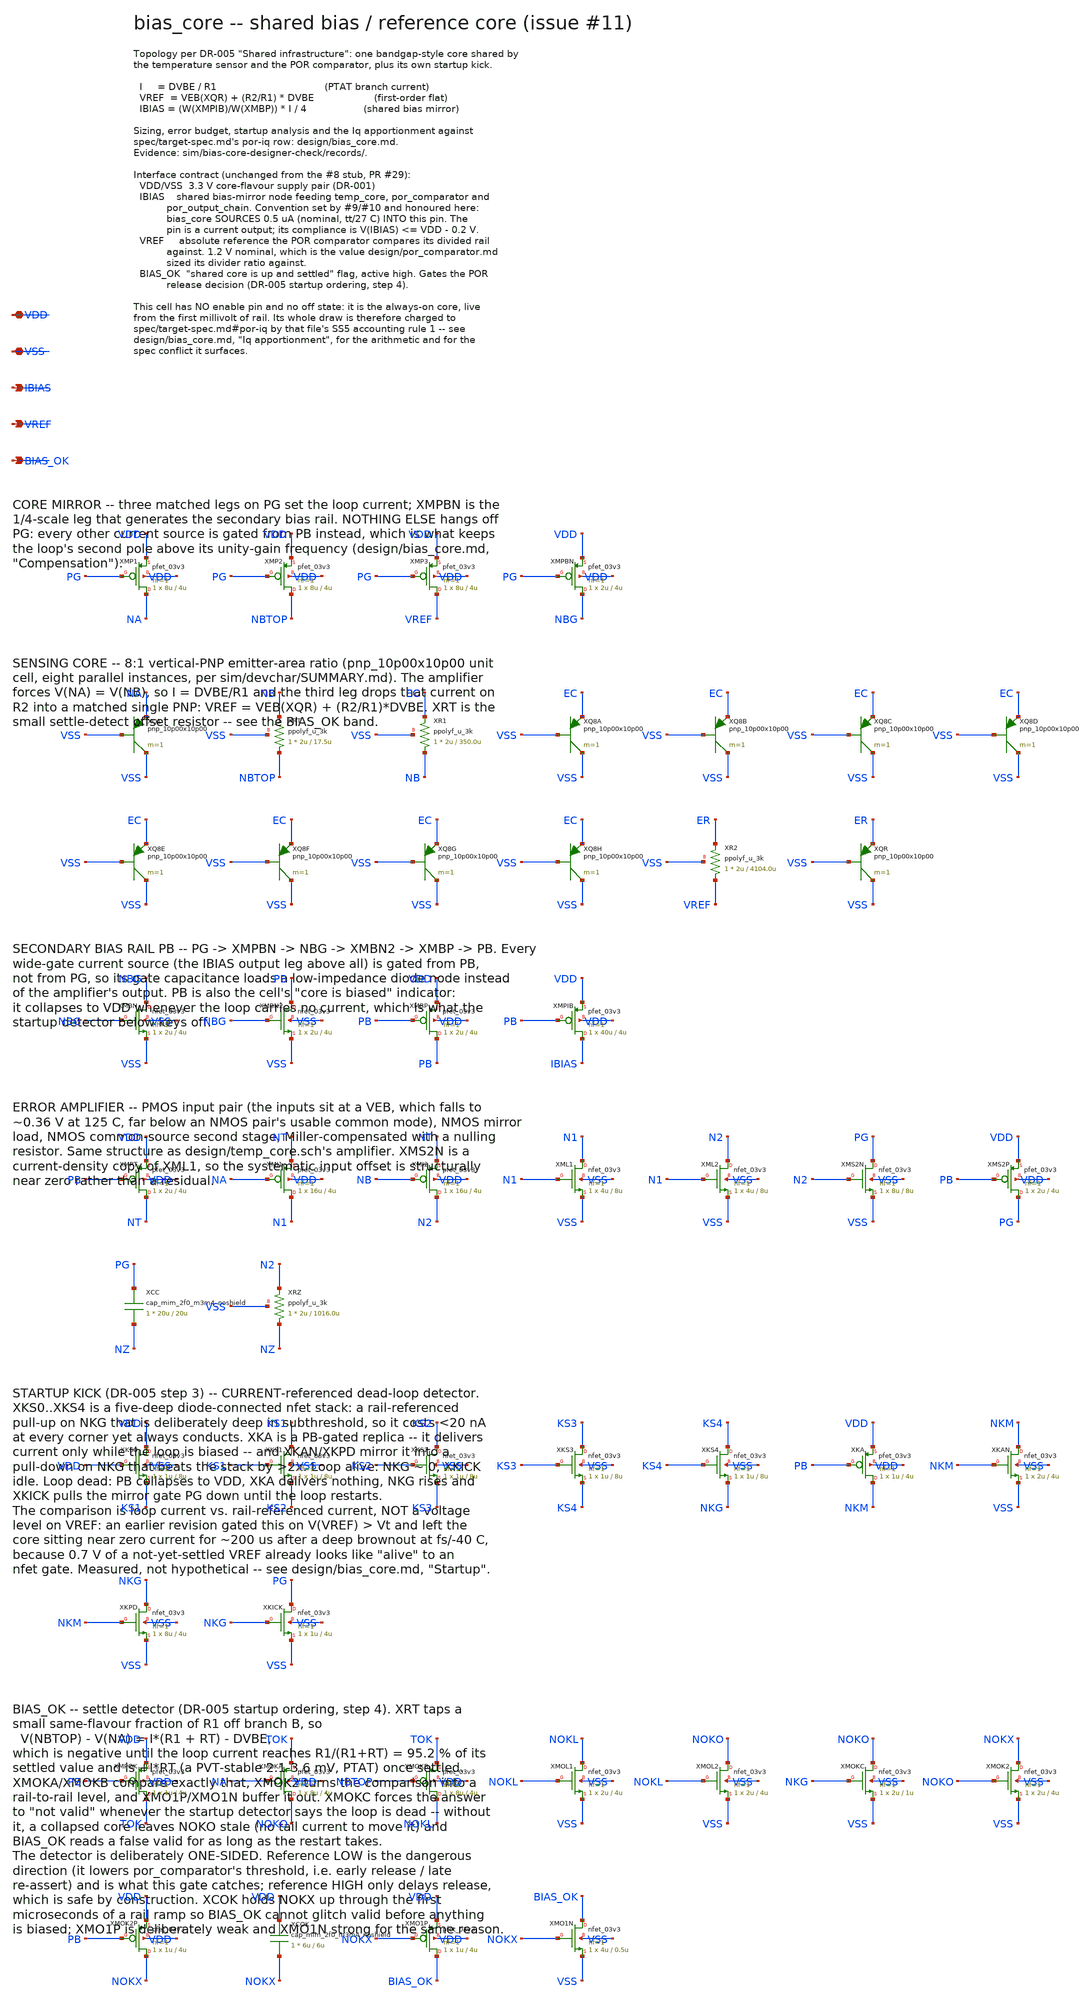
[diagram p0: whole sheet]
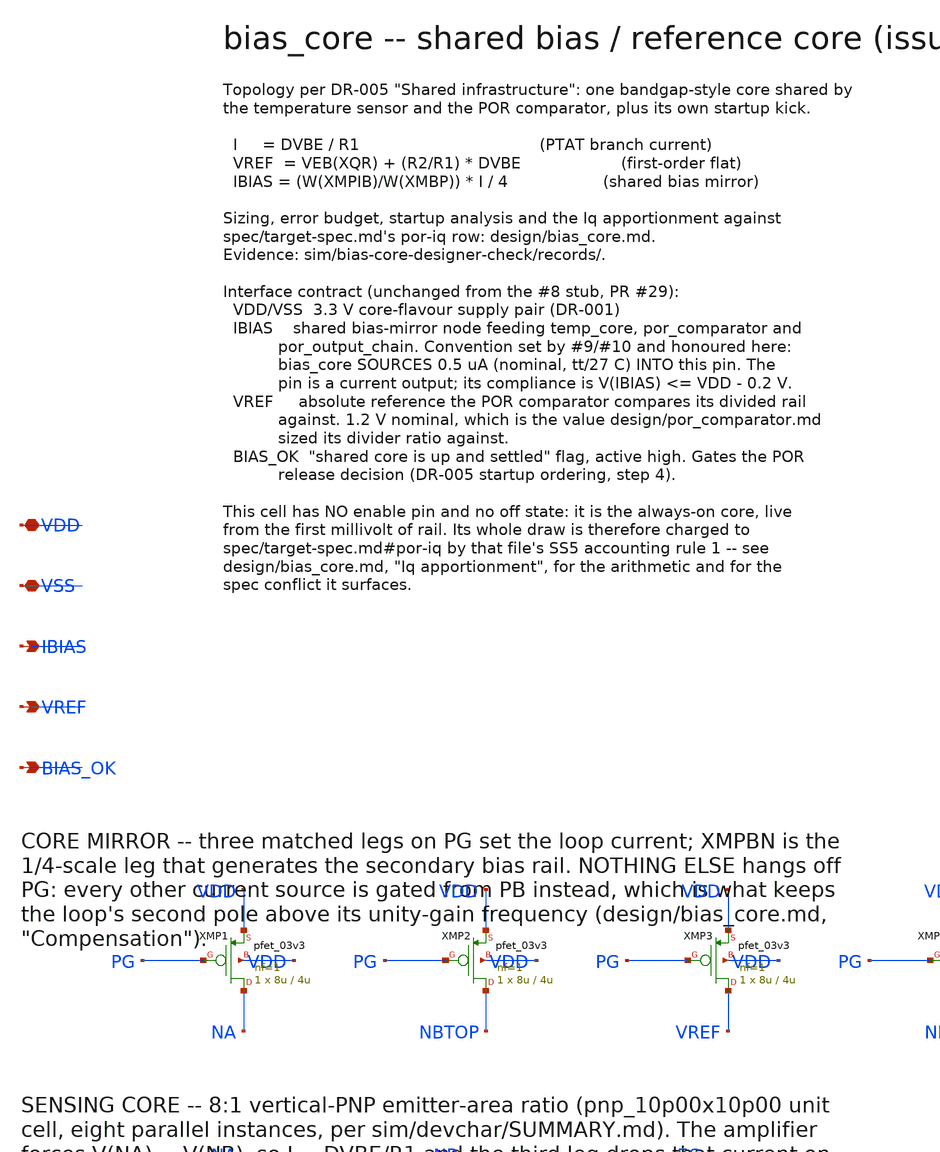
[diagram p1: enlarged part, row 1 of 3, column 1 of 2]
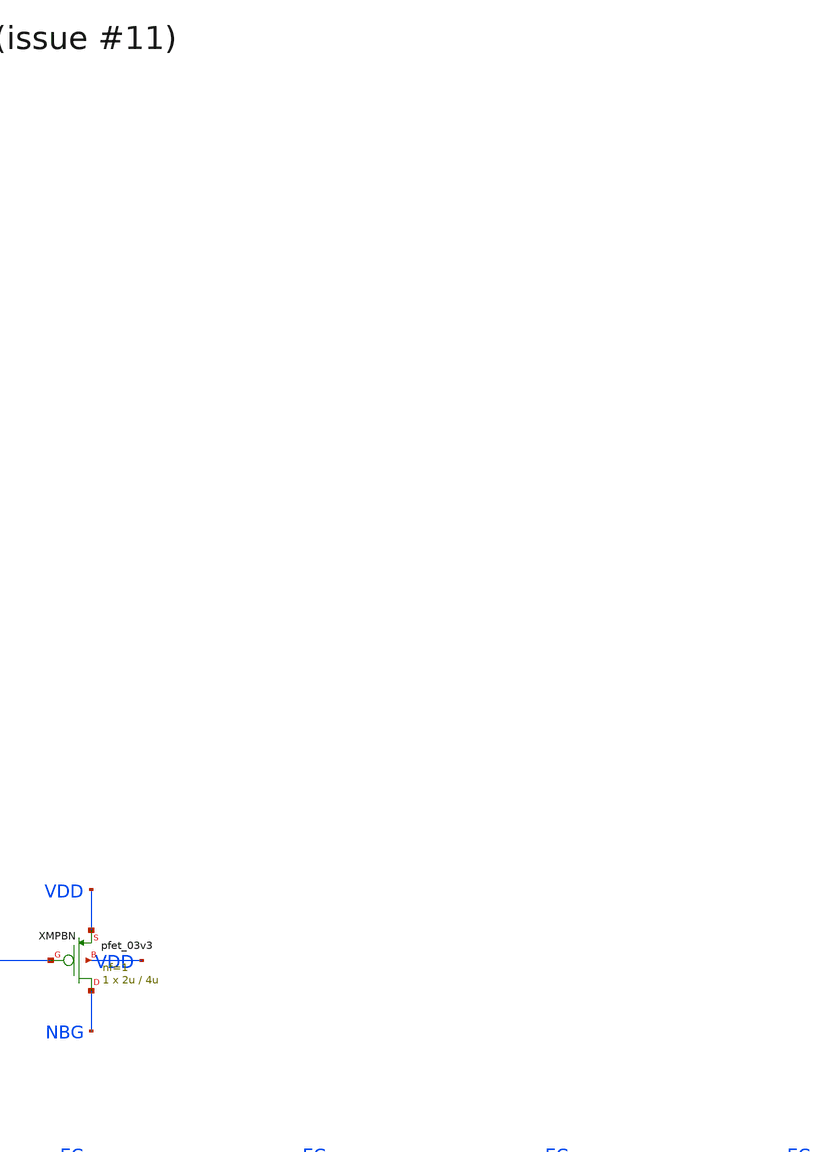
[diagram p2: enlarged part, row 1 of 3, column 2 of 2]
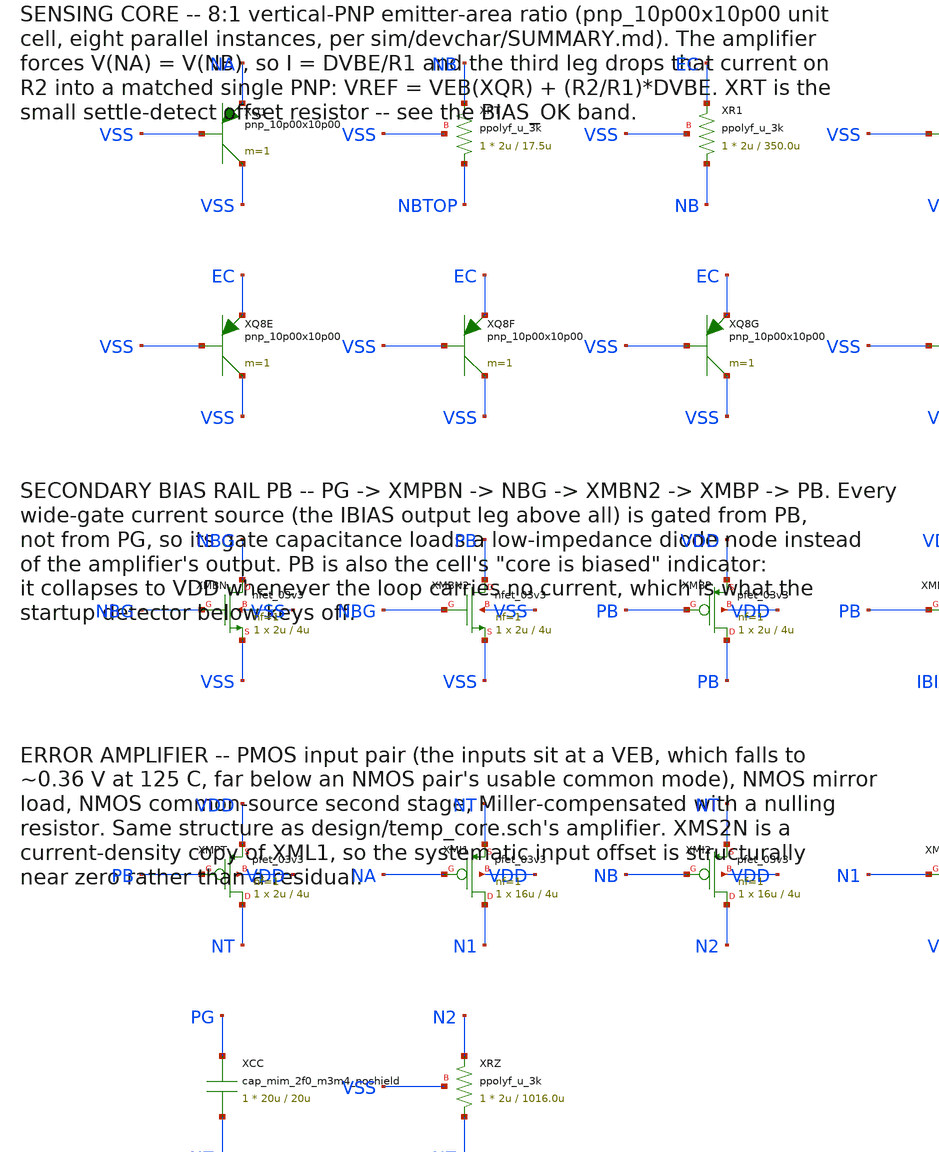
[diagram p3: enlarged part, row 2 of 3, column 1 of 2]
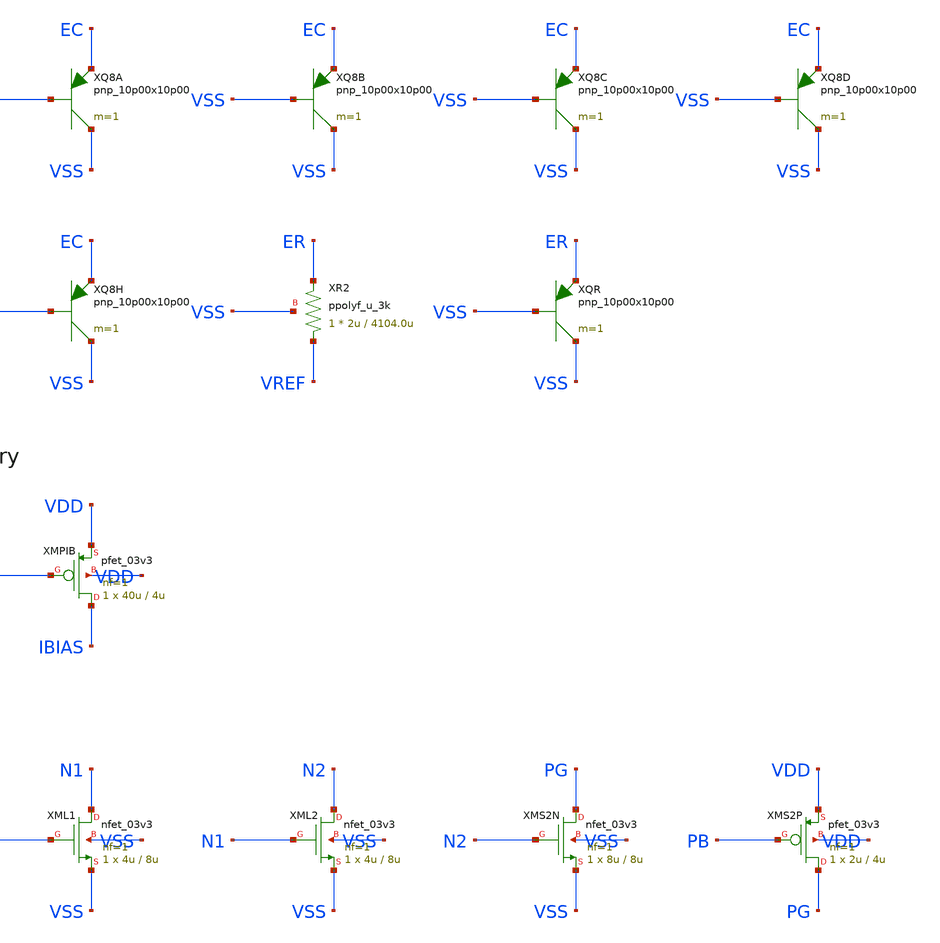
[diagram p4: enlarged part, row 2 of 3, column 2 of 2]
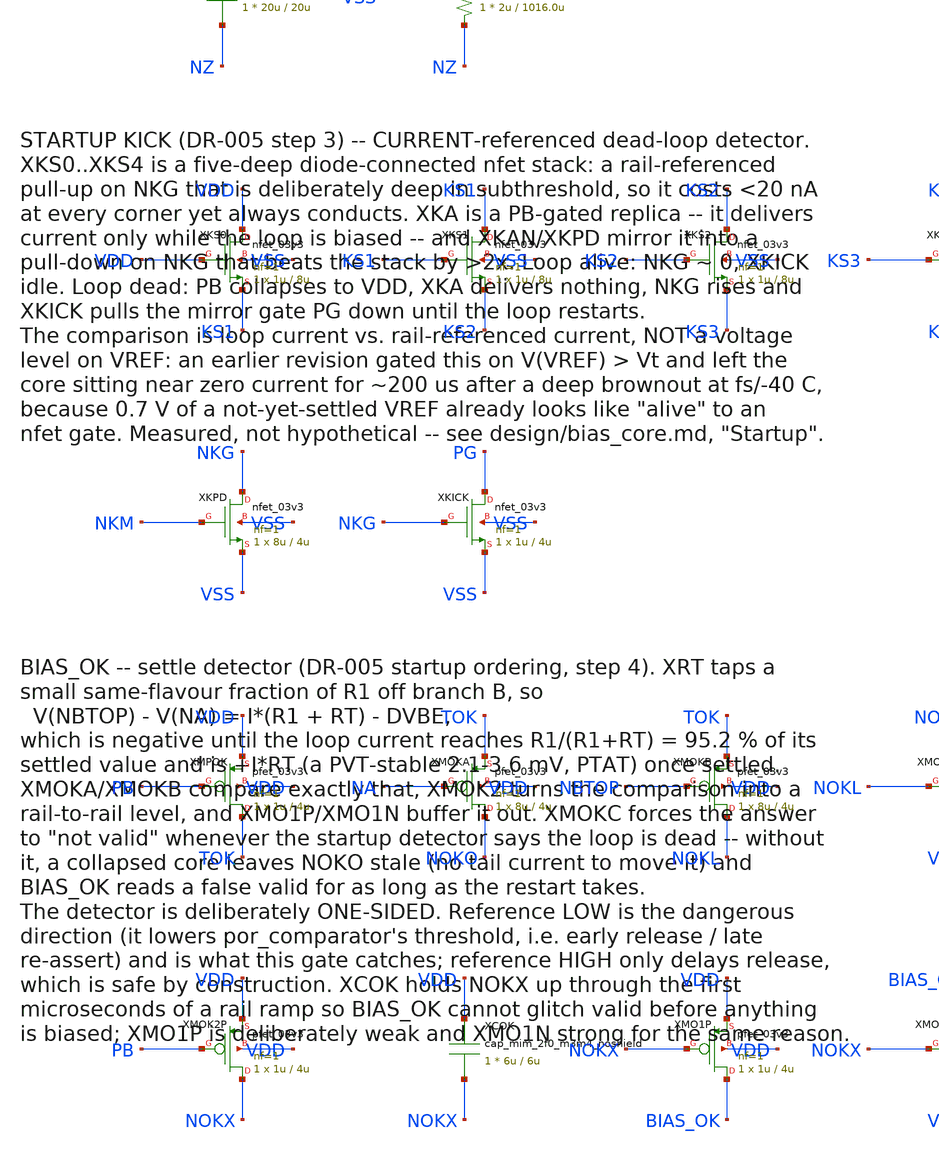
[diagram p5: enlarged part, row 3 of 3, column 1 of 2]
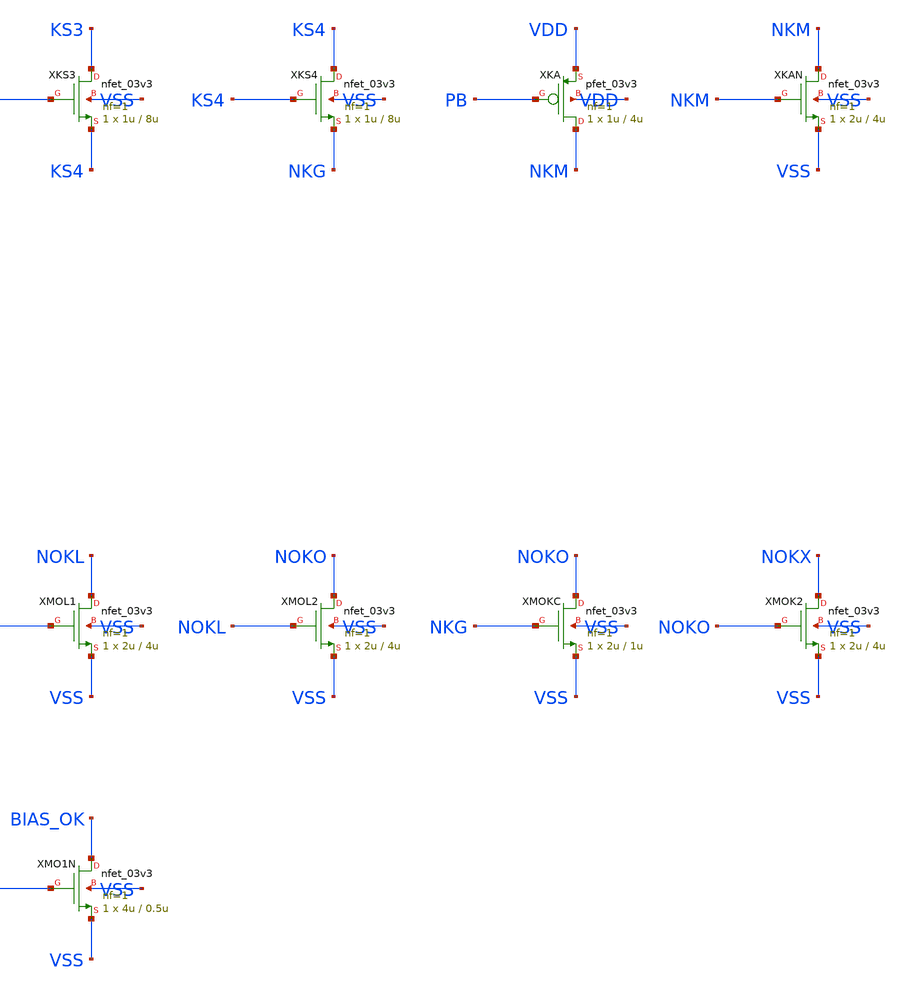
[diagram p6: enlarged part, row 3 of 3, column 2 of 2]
** sch_path: design/bias_core.sch
**.subckt bias_core VDD VSS IBIAS VREF BIAS_OK
*.iopin VDD
*.iopin VSS
*.opin IBIAS
*.opin VREF
*.opin BIAS_OK
XMP1 NA PG VDD VDD pfet_03v3 L=4u W=8u nf=1 ad='int((nf+1)/2) * W/nf * 0.18u' as='int((nf+2)/2) * W/nf * 0.18u'
+ pd='2*int((nf+1)/2) * (W/nf + 0.18u)' ps='2*int((nf+2)/2) * (W/nf + 0.18u)' nrd='0.18u / W' nrs='0.18u / W'
+ sa=0 sb=0 sd=0 m=1
XMP2 NBTOP PG VDD VDD pfet_03v3 L=4u W=8u nf=1 ad='int((nf+1)/2) * W/nf * 0.18u' as='int((nf+2)/2) * W/nf * 0.18u'
+ pd='2*int((nf+1)/2) * (W/nf + 0.18u)' ps='2*int((nf+2)/2) * (W/nf + 0.18u)' nrd='0.18u / W' nrs='0.18u / W'
+ sa=0 sb=0 sd=0 m=1
XMP3 VREF PG VDD VDD pfet_03v3 L=4u W=8u nf=1 ad='int((nf+1)/2) * W/nf * 0.18u' as='int((nf+2)/2) * W/nf * 0.18u'
+ pd='2*int((nf+1)/2) * (W/nf + 0.18u)' ps='2*int((nf+2)/2) * (W/nf + 0.18u)' nrd='0.18u / W' nrs='0.18u / W'
+ sa=0 sb=0 sd=0 m=1
XMPBN NBG PG VDD VDD pfet_03v3 L=4u W=2u nf=1 ad='int((nf+1)/2) * W/nf * 0.18u' as='int((nf+2)/2) * W/nf * 0.18u'
+ pd='2*int((nf+1)/2) * (W/nf + 0.18u)' ps='2*int((nf+2)/2) * (W/nf + 0.18u)' nrd='0.18u / W' nrs='0.18u / W'
+ sa=0 sb=0 sd=0 m=1
XQ1 VSS VSS NA pnp_10p00x10p00 m=1
XRT NBTOP NB VSS ppolyf_u_3k r_width=2u r_length=17.5u m=1
XR1 NB EC VSS ppolyf_u_3k r_width=2u r_length=350.0u m=1
XQ8A VSS VSS EC pnp_10p00x10p00 m=1
XQ8B VSS VSS EC pnp_10p00x10p00 m=1
XQ8C VSS VSS EC pnp_10p00x10p00 m=1
XQ8D VSS VSS EC pnp_10p00x10p00 m=1
XQ8E VSS VSS EC pnp_10p00x10p00 m=1
XQ8F VSS VSS EC pnp_10p00x10p00 m=1
XQ8G VSS VSS EC pnp_10p00x10p00 m=1
XQ8H VSS VSS EC pnp_10p00x10p00 m=1
XR2 VREF ER VSS ppolyf_u_3k r_width=2u r_length=4104.0u m=1
XQR VSS VSS ER pnp_10p00x10p00 m=1
XMBN NBG NBG VSS VSS nfet_03v3 L=4u W=2u nf=1 ad='int((nf+1)/2) * W/nf * 0.18u' as='int((nf+2)/2) * W/nf * 0.18u'
+ pd='2*int((nf+1)/2) * (W/nf + 0.18u)' ps='2*int((nf+2)/2) * (W/nf + 0.18u)' nrd='0.18u / W' nrs='0.18u / W'
+ sa=0 sb=0 sd=0 m=1
XMBN2 PB NBG VSS VSS nfet_03v3 L=4u W=2u nf=1 ad='int((nf+1)/2) * W/nf * 0.18u' as='int((nf+2)/2) * W/nf * 0.18u'
+ pd='2*int((nf+1)/2) * (W/nf + 0.18u)' ps='2*int((nf+2)/2) * (W/nf + 0.18u)' nrd='0.18u / W' nrs='0.18u / W'
+ sa=0 sb=0 sd=0 m=1
XMBP PB PB VDD VDD pfet_03v3 L=4u W=2u nf=1 ad='int((nf+1)/2) * W/nf * 0.18u' as='int((nf+2)/2) * W/nf * 0.18u'
+ pd='2*int((nf+1)/2) * (W/nf + 0.18u)' ps='2*int((nf+2)/2) * (W/nf + 0.18u)' nrd='0.18u / W' nrs='0.18u / W'
+ sa=0 sb=0 sd=0 m=1
XMPIB IBIAS PB VDD VDD pfet_03v3 L=4u W=40u nf=1 ad='int((nf+1)/2) * W/nf * 0.18u' as='int((nf+2)/2) * W/nf * 0.18u'
+ pd='2*int((nf+1)/2) * (W/nf + 0.18u)' ps='2*int((nf+2)/2) * (W/nf + 0.18u)' nrd='0.18u / W' nrs='0.18u / W'
+ sa=0 sb=0 sd=0 m=1
XMPT NT PB VDD VDD pfet_03v3 L=4u W=2u nf=1 ad='int((nf+1)/2) * W/nf * 0.18u' as='int((nf+2)/2) * W/nf * 0.18u'
+ pd='2*int((nf+1)/2) * (W/nf + 0.18u)' ps='2*int((nf+2)/2) * (W/nf + 0.18u)' nrd='0.18u / W' nrs='0.18u / W'
+ sa=0 sb=0 sd=0 m=1
XMI1 N1 NA NT VDD pfet_03v3 L=4u W=16u nf=1 ad='int((nf+1)/2) * W/nf * 0.18u' as='int((nf+2)/2) * W/nf * 0.18u'
+ pd='2*int((nf+1)/2) * (W/nf + 0.18u)' ps='2*int((nf+2)/2) * (W/nf + 0.18u)' nrd='0.18u / W' nrs='0.18u / W'
+ sa=0 sb=0 sd=0 m=1
XMI2 N2 NB NT VDD pfet_03v3 L=4u W=16u nf=1 ad='int((nf+1)/2) * W/nf * 0.18u' as='int((nf+2)/2) * W/nf * 0.18u'
+ pd='2*int((nf+1)/2) * (W/nf + 0.18u)' ps='2*int((nf+2)/2) * (W/nf + 0.18u)' nrd='0.18u / W' nrs='0.18u / W'
+ sa=0 sb=0 sd=0 m=1
XML1 N1 N1 VSS VSS nfet_03v3 L=8u W=4u nf=1 ad='int((nf+1)/2) * W/nf * 0.18u' as='int((nf+2)/2) * W/nf * 0.18u'
+ pd='2*int((nf+1)/2) * (W/nf + 0.18u)' ps='2*int((nf+2)/2) * (W/nf + 0.18u)' nrd='0.18u / W' nrs='0.18u / W'
+ sa=0 sb=0 sd=0 m=1
XML2 N2 N1 VSS VSS nfet_03v3 L=8u W=4u nf=1 ad='int((nf+1)/2) * W/nf * 0.18u' as='int((nf+2)/2) * W/nf * 0.18u'
+ pd='2*int((nf+1)/2) * (W/nf + 0.18u)' ps='2*int((nf+2)/2) * (W/nf + 0.18u)' nrd='0.18u / W' nrs='0.18u / W'
+ sa=0 sb=0 sd=0 m=1
XMS2N PG N2 VSS VSS nfet_03v3 L=8u W=8u nf=1 ad='int((nf+1)/2) * W/nf * 0.18u' as='int((nf+2)/2) * W/nf * 0.18u'
+ pd='2*int((nf+1)/2) * (W/nf + 0.18u)' ps='2*int((nf+2)/2) * (W/nf + 0.18u)' nrd='0.18u / W' nrs='0.18u / W'
+ sa=0 sb=0 sd=0 m=1
XMS2P PG PB VDD VDD pfet_03v3 L=4u W=2u nf=1 ad='int((nf+1)/2) * W/nf * 0.18u' as='int((nf+2)/2) * W/nf * 0.18u'
+ pd='2*int((nf+1)/2) * (W/nf + 0.18u)' ps='2*int((nf+2)/2) * (W/nf + 0.18u)' nrd='0.18u / W' nrs='0.18u / W'
+ sa=0 sb=0 sd=0 m=1
XCC PG NZ cap_mim_2f0_m3m4_noshield c_width=20u c_length=20u m=1
XRZ NZ N2 VSS ppolyf_u_3k r_width=2u r_length=1016.0u m=1
XKS0 VDD VDD KS1 VSS nfet_03v3 L=8u W=1u nf=1 ad='int((nf+1)/2) * W/nf * 0.18u' as='int((nf+2)/2) * W/nf * 0.18u'
+ pd='2*int((nf+1)/2) * (W/nf + 0.18u)' ps='2*int((nf+2)/2) * (W/nf + 0.18u)' nrd='0.18u / W' nrs='0.18u / W'
+ sa=0 sb=0 sd=0 m=1
XKS1 KS1 KS1 KS2 VSS nfet_03v3 L=8u W=1u nf=1 ad='int((nf+1)/2) * W/nf * 0.18u' as='int((nf+2)/2) * W/nf * 0.18u'
+ pd='2*int((nf+1)/2) * (W/nf + 0.18u)' ps='2*int((nf+2)/2) * (W/nf + 0.18u)' nrd='0.18u / W' nrs='0.18u / W'
+ sa=0 sb=0 sd=0 m=1
XKS2 KS2 KS2 KS3 VSS nfet_03v3 L=8u W=1u nf=1 ad='int((nf+1)/2) * W/nf * 0.18u' as='int((nf+2)/2) * W/nf * 0.18u'
+ pd='2*int((nf+1)/2) * (W/nf + 0.18u)' ps='2*int((nf+2)/2) * (W/nf + 0.18u)' nrd='0.18u / W' nrs='0.18u / W'
+ sa=0 sb=0 sd=0 m=1
XKS3 KS3 KS3 KS4 VSS nfet_03v3 L=8u W=1u nf=1 ad='int((nf+1)/2) * W/nf * 0.18u' as='int((nf+2)/2) * W/nf * 0.18u'
+ pd='2*int((nf+1)/2) * (W/nf + 0.18u)' ps='2*int((nf+2)/2) * (W/nf + 0.18u)' nrd='0.18u / W' nrs='0.18u / W'
+ sa=0 sb=0 sd=0 m=1
XKS4 KS4 KS4 NKG VSS nfet_03v3 L=8u W=1u nf=1 ad='int((nf+1)/2) * W/nf * 0.18u' as='int((nf+2)/2) * W/nf * 0.18u'
+ pd='2*int((nf+1)/2) * (W/nf + 0.18u)' ps='2*int((nf+2)/2) * (W/nf + 0.18u)' nrd='0.18u / W' nrs='0.18u / W'
+ sa=0 sb=0 sd=0 m=1
XKA NKM PB VDD VDD pfet_03v3 L=4u W=1u nf=1 ad='int((nf+1)/2) * W/nf * 0.18u' as='int((nf+2)/2) * W/nf * 0.18u'
+ pd='2*int((nf+1)/2) * (W/nf + 0.18u)' ps='2*int((nf+2)/2) * (W/nf + 0.18u)' nrd='0.18u / W' nrs='0.18u / W'
+ sa=0 sb=0 sd=0 m=1
XKAN NKM NKM VSS VSS nfet_03v3 L=4u W=2u nf=1 ad='int((nf+1)/2) * W/nf * 0.18u' as='int((nf+2)/2) * W/nf * 0.18u'
+ pd='2*int((nf+1)/2) * (W/nf + 0.18u)' ps='2*int((nf+2)/2) * (W/nf + 0.18u)' nrd='0.18u / W' nrs='0.18u / W'
+ sa=0 sb=0 sd=0 m=1
XKPD NKG NKM VSS VSS nfet_03v3 L=4u W=8u nf=1 ad='int((nf+1)/2) * W/nf * 0.18u' as='int((nf+2)/2) * W/nf * 0.18u'
+ pd='2*int((nf+1)/2) * (W/nf + 0.18u)' ps='2*int((nf+2)/2) * (W/nf + 0.18u)' nrd='0.18u / W' nrs='0.18u / W'
+ sa=0 sb=0 sd=0 m=1
XKICK PG NKG VSS VSS nfet_03v3 L=4u W=1u nf=1 ad='int((nf+1)/2) * W/nf * 0.18u' as='int((nf+2)/2) * W/nf * 0.18u'
+ pd='2*int((nf+1)/2) * (W/nf + 0.18u)' ps='2*int((nf+2)/2) * (W/nf + 0.18u)' nrd='0.18u / W' nrs='0.18u / W'
+ sa=0 sb=0 sd=0 m=1
XMPOK TOK PB VDD VDD pfet_03v3 L=4u W=1u nf=1 ad='int((nf+1)/2) * W/nf * 0.18u' as='int((nf+2)/2) * W/nf * 0.18u'
+ pd='2*int((nf+1)/2) * (W/nf + 0.18u)' ps='2*int((nf+2)/2) * (W/nf + 0.18u)' nrd='0.18u / W' nrs='0.18u / W'
+ sa=0 sb=0 sd=0 m=1
XMOKA NOKO NA TOK VDD pfet_03v3 L=4u W=8u nf=1 ad='int((nf+1)/2) * W/nf * 0.18u' as='int((nf+2)/2) * W/nf * 0.18u'
+ pd='2*int((nf+1)/2) * (W/nf + 0.18u)' ps='2*int((nf+2)/2) * (W/nf + 0.18u)' nrd='0.18u / W' nrs='0.18u / W'
+ sa=0 sb=0 sd=0 m=1
XMOKB NOKL NBTOP TOK VDD pfet_03v3 L=4u W=8u nf=1 ad='int((nf+1)/2) * W/nf * 0.18u' as='int((nf+2)/2) * W/nf * 0.18u'
+ pd='2*int((nf+1)/2) * (W/nf + 0.18u)' ps='2*int((nf+2)/2) * (W/nf + 0.18u)' nrd='0.18u / W' nrs='0.18u / W'
+ sa=0 sb=0 sd=0 m=1
XMOL1 NOKL NOKL VSS VSS nfet_03v3 L=4u W=2u nf=1 ad='int((nf+1)/2) * W/nf * 0.18u' as='int((nf+2)/2) * W/nf * 0.18u'
+ pd='2*int((nf+1)/2) * (W/nf + 0.18u)' ps='2*int((nf+2)/2) * (W/nf + 0.18u)' nrd='0.18u / W' nrs='0.18u / W'
+ sa=0 sb=0 sd=0 m=1
XMOL2 NOKO NOKL VSS VSS nfet_03v3 L=4u W=2u nf=1 ad='int((nf+1)/2) * W/nf * 0.18u' as='int((nf+2)/2) * W/nf * 0.18u'
+ pd='2*int((nf+1)/2) * (W/nf + 0.18u)' ps='2*int((nf+2)/2) * (W/nf + 0.18u)' nrd='0.18u / W' nrs='0.18u / W'
+ sa=0 sb=0 sd=0 m=1
XMOKC NOKO NKG VSS VSS nfet_03v3 L=1u W=2u nf=1 ad='int((nf+1)/2) * W/nf * 0.18u' as='int((nf+2)/2) * W/nf * 0.18u'
+ pd='2*int((nf+1)/2) * (W/nf + 0.18u)' ps='2*int((nf+2)/2) * (W/nf + 0.18u)' nrd='0.18u / W' nrs='0.18u / W'
+ sa=0 sb=0 sd=0 m=1
XMOK2 NOKX NOKO VSS VSS nfet_03v3 L=4u W=2u nf=1 ad='int((nf+1)/2) * W/nf * 0.18u' as='int((nf+2)/2) * W/nf * 0.18u'
+ pd='2*int((nf+1)/2) * (W/nf + 0.18u)' ps='2*int((nf+2)/2) * (W/nf + 0.18u)' nrd='0.18u / W' nrs='0.18u / W'
+ sa=0 sb=0 sd=0 m=1
XMOK2P NOKX PB VDD VDD pfet_03v3 L=4u W=1u nf=1 ad='int((nf+1)/2) * W/nf * 0.18u' as='int((nf+2)/2) * W/nf * 0.18u'
+ pd='2*int((nf+1)/2) * (W/nf + 0.18u)' ps='2*int((nf+2)/2) * (W/nf + 0.18u)' nrd='0.18u / W' nrs='0.18u / W'
+ sa=0 sb=0 sd=0 m=1
XCOK VDD NOKX cap_mim_2f0_m3m4_noshield c_width=6u c_length=6u m=1
XMO1P BIAS_OK NOKX VDD VDD pfet_03v3 L=4u W=1u nf=1 ad='int((nf+1)/2) * W/nf * 0.18u' as='int((nf+2)/2) * W/nf * 0.18u'
+ pd='2*int((nf+1)/2) * (W/nf + 0.18u)' ps='2*int((nf+2)/2) * (W/nf + 0.18u)' nrd='0.18u / W' nrs='0.18u / W'
+ sa=0 sb=0 sd=0 m=1
XMO1N BIAS_OK NOKX VSS VSS nfet_03v3 L=0.5u W=4u nf=1 ad='int((nf+1)/2) * W/nf * 0.18u' as='int((nf+2)/2) * W/nf * 0.18u'
+ pd='2*int((nf+1)/2) * (W/nf + 0.18u)' ps='2*int((nf+2)/2) * (W/nf + 0.18u)' nrd='0.18u / W' nrs='0.18u / W'
+ sa=0 sb=0 sd=0 m=1
**.ends
.end
